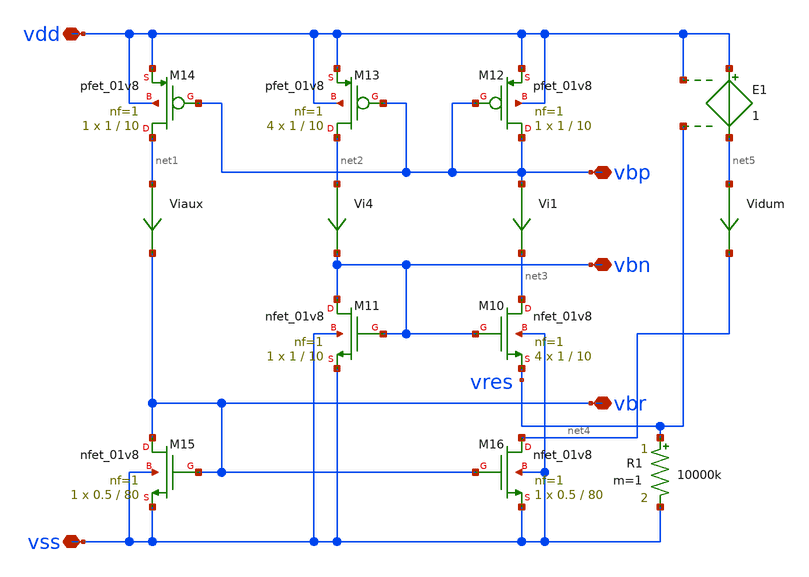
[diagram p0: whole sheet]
** sch_path: playground/OgueyAebischerBias.sch
**.subckt OgueyAebischerBias vss vdd vbp vbn vbr
*.iopin vss
*.iopin vdd
*.iopin vbp
*.iopin vbn
*.iopin vbr
XM10 net3 vbn vres vss sky130_fd_pr__nfet_01v8 L=10 W=1 nf=1 ad='int((1 + 1)/2) * 1 / 1 * 0.29' as='int((1 + 2)/2) * 1 / 1 * 0.29'
+ pd='2*int((1 + 1)/2) * (1 / 1 + 0.29)' ps='2*int((1 + 2)/2) * (1 / 1 + 0.29)' nrd='0.29 / 1 ' nrs='0.29 / 1 '
+ sa=0 sb=0 sd=0 mult=4 m=4
XM12 vbp vbp vdd vdd sky130_fd_pr__pfet_01v8 L=10 W=1 nf=1 ad='int((nf+1)/2) * W/nf * 0.29' as='int((nf+2)/2) * W/nf * 0.29'
+ pd='2*int((nf+1)/2) * (W/nf + 0.29)' ps='2*int((nf+2)/2) * (W/nf + 0.29)' nrd='0.29 / W' nrs='0.29 / W'
+ sa=0 sb=0 sd=0 mult=1 m=1
XM11 vbn vbn vss vss sky130_fd_pr__nfet_01v8 L=10 W=1 nf=1 ad='int((1 + 1)/2) * 1 / 1 * 0.29' as='int((1 + 2)/2) * 1 / 1 * 0.29'
+ pd='2*int((1 + 1)/2) * (1 / 1 + 0.29)' ps='2*int((1 + 2)/2) * (1 / 1 + 0.29)' nrd='0.29 / 1 ' nrs='0.29 / 1 '
+ sa=0 sb=0 sd=0 mult=1 m=1
XM13 net2 vbp vdd vdd sky130_fd_pr__pfet_01v8 L=10 W=1 nf=1 ad='int((nf+1)/2) * W/nf * 0.29' as='int((nf+2)/2) * W/nf * 0.29'
+ pd='2*int((nf+1)/2) * (W/nf + 0.29)' ps='2*int((nf+2)/2) * (W/nf + 0.29)' nrd='0.29 / W' nrs='0.29 / W'
+ sa=0 sb=0 sd=0 mult=4 m=4
XM14 net1 vbp vdd vdd sky130_fd_pr__pfet_01v8 L=10 W=1 nf=1 ad='int((nf+1)/2) * W/nf * 0.29' as='int((nf+2)/2) * W/nf * 0.29'
+ pd='2*int((nf+1)/2) * (W/nf + 0.29)' ps='2*int((nf+2)/2) * (W/nf + 0.29)' nrd='0.29 / W' nrs='0.29 / W'
+ sa=0 sb=0 sd=0 mult=1 m=1
XM16 net4 vbr vss vss sky130_fd_pr__nfet_01v8 L=80 W=0.5 nf=1 ad='int((1 + 1)/2) * 0.5 / 1 * 0.29' as='int((1 + 2)/2) * 0.5 / 1 * 0.29'
+ pd='2*int((1 + 1)/2) * (0.5 / 1 + 0.29)' ps='2*int((1 + 2)/2) * (0.5 / 1 + 0.29)' nrd='0.29 / 0.5 ' nrs='0.29 / 0.5 '
+ sa=0 sb=0 sd=0 mult=1 m=1
XM15 vbr vbr vss vss sky130_fd_pr__nfet_01v8 L=80 W=0.5 nf=1 ad='int((1 + 1)/2) * 0.5 / 1 * 0.29' as='int((1 + 2)/2) * 0.5 / 1 * 0.29'
+ pd='2*int((1 + 1)/2) * (0.5 / 1 + 0.29)' ps='2*int((1 + 2)/2) * (0.5 / 1 + 0.29)' nrd='0.29 / 0.5 ' nrs='0.29 / 0.5 '
+ sa=0 sb=0 sd=0 mult=1 m=1
Vi1 vbp net3 0
.save i(vi1)
Vi4 net2 vbn 0
.save i(vi4)
Viaux net1 vbr 0
.save i(viaux)
R1 vres vss 10000k m=1
Vidum net5 net4 0
.save i(vidum)
E1 vdd net5 vdd vres 1
**.ends
.end
